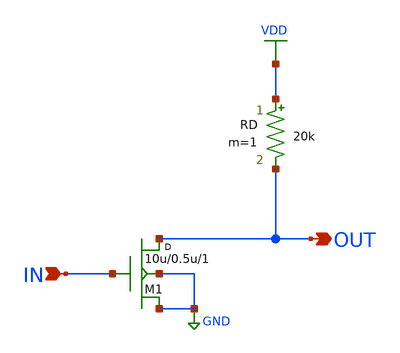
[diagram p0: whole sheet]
** sch_path: E3_238_Analog_VLSI_Circuits/06_Single_Stage_Amplifiers/cs_resistive_load.sch
**.subckt cs_resistive_load IN OUT
*.ipin IN
*.opin OUT
M1 OUT IN GND GND nmos w=10u l=0.5u m=1
RD VDD OUT 20k m=1
**** begin user architecture code

.include /home/anirudh/Analog_VLSI_Projects/models/cmos_180nm.mod
VDD VDD 0 DC 1.8
VIN IN 0 DC 0.57 AC 1
CL OUT GND 1p

.control
  op
  print v(OUT)
  ac dec 20 1 1G
  plot db(v(OUT))
  plot phase(v(OUT))*180/pi
.endc


**** end user architecture code
**.ends
.GLOBAL VDD
.GLOBAL GND
.end
